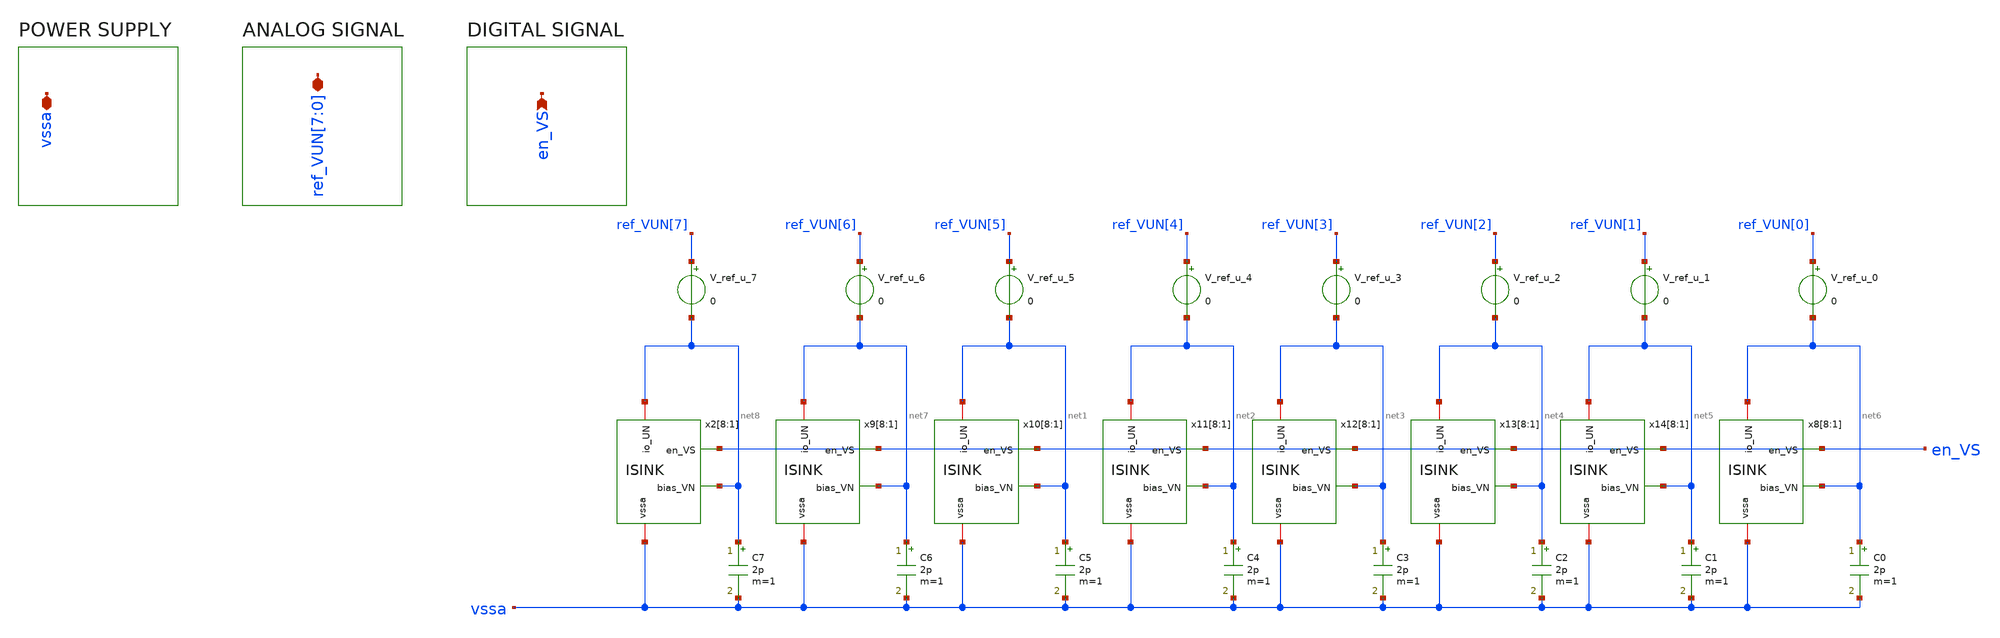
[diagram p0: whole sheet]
** sch_path: CoreDiodeT.sch
**.subckt CoreDiodeT
*+ ref_VUN[7],ref_VUN[6],ref_VUN[5],ref_VUN[4],ref_VUN[3],ref_VUN[2],ref_VUN[1],ref_VUN[0] en_VS vssa
*.iopin ref_VUN[7],ref_VUN[6],ref_VUN[5],ref_VUN[4],ref_VUN[3],ref_VUN[2],ref_VUN[1],ref_VUN[0]
*.ipin en_VS
*.iopin vssa
x2[8] net8 vssa en_VS net8 ISINK
x2[7] net8 vssa en_VS net8 ISINK
x2[6] net8 vssa en_VS net8 ISINK
x2[5] net8 vssa en_VS net8 ISINK
x2[4] net8 vssa en_VS net8 ISINK
x2[3] net8 vssa en_VS net8 ISINK
x2[2] net8 vssa en_VS net8 ISINK
x2[1] net8 vssa en_VS net8 ISINK
x9[8] net7 vssa en_VS net7 ISINK
x9[7] net7 vssa en_VS net7 ISINK
x9[6] net7 vssa en_VS net7 ISINK
x9[5] net7 vssa en_VS net7 ISINK
x9[4] net7 vssa en_VS net7 ISINK
x9[3] net7 vssa en_VS net7 ISINK
x9[2] net7 vssa en_VS net7 ISINK
x9[1] net7 vssa en_VS net7 ISINK
x10[8] net1 vssa en_VS net1 ISINK
x10[7] net1 vssa en_VS net1 ISINK
x10[6] net1 vssa en_VS net1 ISINK
x10[5] net1 vssa en_VS net1 ISINK
x10[4] net1 vssa en_VS net1 ISINK
x10[3] net1 vssa en_VS net1 ISINK
x10[2] net1 vssa en_VS net1 ISINK
x10[1] net1 vssa en_VS net1 ISINK
x11[8] net2 vssa en_VS net2 ISINK
x11[7] net2 vssa en_VS net2 ISINK
x11[6] net2 vssa en_VS net2 ISINK
x11[5] net2 vssa en_VS net2 ISINK
x11[4] net2 vssa en_VS net2 ISINK
x11[3] net2 vssa en_VS net2 ISINK
x11[2] net2 vssa en_VS net2 ISINK
x11[1] net2 vssa en_VS net2 ISINK
x12[8] net3 vssa en_VS net3 ISINK
x12[7] net3 vssa en_VS net3 ISINK
x12[6] net3 vssa en_VS net3 ISINK
x12[5] net3 vssa en_VS net3 ISINK
x12[4] net3 vssa en_VS net3 ISINK
x12[3] net3 vssa en_VS net3 ISINK
x12[2] net3 vssa en_VS net3 ISINK
x12[1] net3 vssa en_VS net3 ISINK
x13[8] net4 vssa en_VS net4 ISINK
x13[7] net4 vssa en_VS net4 ISINK
x13[6] net4 vssa en_VS net4 ISINK
x13[5] net4 vssa en_VS net4 ISINK
x13[4] net4 vssa en_VS net4 ISINK
x13[3] net4 vssa en_VS net4 ISINK
x13[2] net4 vssa en_VS net4 ISINK
x13[1] net4 vssa en_VS net4 ISINK
x14[8] net5 vssa en_VS net5 ISINK
x14[7] net5 vssa en_VS net5 ISINK
x14[6] net5 vssa en_VS net5 ISINK
x14[5] net5 vssa en_VS net5 ISINK
x14[4] net5 vssa en_VS net5 ISINK
x14[3] net5 vssa en_VS net5 ISINK
x14[2] net5 vssa en_VS net5 ISINK
x14[1] net5 vssa en_VS net5 ISINK
x8[8] net6 vssa en_VS net6 ISINK
x8[7] net6 vssa en_VS net6 ISINK
x8[6] net6 vssa en_VS net6 ISINK
x8[5] net6 vssa en_VS net6 ISINK
x8[4] net6 vssa en_VS net6 ISINK
x8[3] net6 vssa en_VS net6 ISINK
x8[2] net6 vssa en_VS net6 ISINK
x8[1] net6 vssa en_VS net6 ISINK
C0 net6 vssa 2p m=1
C1 net5 vssa 2p m=1
C2 net4 vssa 2p m=1
C3 net3 vssa 2p m=1
C4 net2 vssa 2p m=1
C5 net1 vssa 2p m=1
C6 net7 vssa 2p m=1
C7 net8 vssa 2p m=1
V_ref_u_0 ref_VUN[0] net6 0
V_ref_u_1 ref_VUN[1] net5 0
V_ref_u_2 ref_VUN[2] net4 0
V_ref_u_3 ref_VUN[3] net3 0
V_ref_u_4 ref_VUN[4] net2 0
V_ref_u_5 ref_VUN[5] net1 0
V_ref_u_6 ref_VUN[6] net7 0
V_ref_u_7 ref_VUN[7] net8 0
**.ends

* expanding   symbol:  ISINK.sym # of pins=4
** sym_path: ISINK.sym
** sch_path: ISINK.sch
.subckt ISINK bias_VN vssa en_VS io_UN
*.ipin en_VS
*.iopin vssa
*.ipin bias_VN
*.iopin io_UN
XM1 io_UN en_VS net2 vssa sg13_hv_nmos w=2.5u l=0.5u ng=1 m=1 mm_ok=1
XM2 net2 bias_VN net1 vssa sg13_hv_nmos w=1u l=4u ng=1 m=1 mm_ok=1
XM3 net1 bias_VN vssa vssa sg13_hv_nmos w=1u l=4u ng=1 m=1 mm_ok=1
.ends

.end
